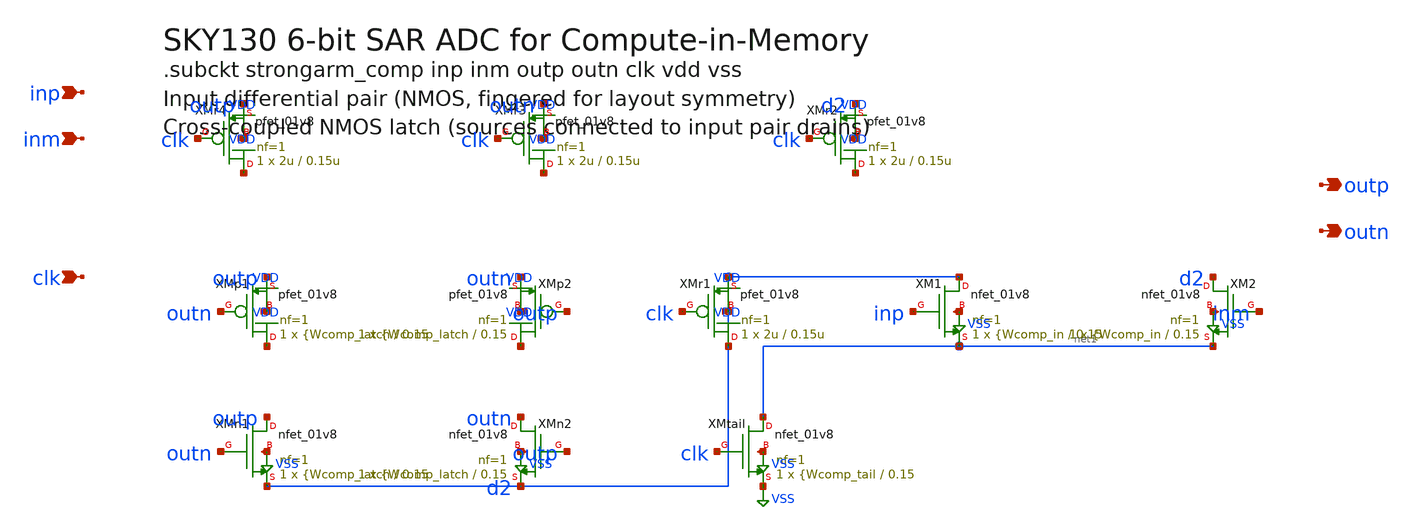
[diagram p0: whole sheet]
** sch_path: data/sch/cim_adc.sch
**.subckt cim_adc inp inm outp outn clk
*.ipin inp
*.ipin inm
*.opin outp
*.opin outn
*.ipin clk
XXMtail net1 clk VSS VSS sky130_fd_pr__nfet_01v8 L=0.15 W={Wcomp_tail nf=1 ad='int((1 + 1)/2) * {Wcomp_tail / 1 * 0.29'
+ as='int((1 + 2)/2) * {Wcomp_tail / 1 * 0.29' pd='2*int((1 + 1)/2) * ({Wcomp_tail / 1 + 0.29)' ps='2*int((1 + 2)/2) * ({Wcomp_tail
+ / 1 + 0.29)' nrd='0.29 / {Wcomp_tail ' nrs='0.29 / {Wcomp_tail ' sa=0 sb=0 sd=0 mult=1 m=1
XXM1 d2 inp net1 VSS sky130_fd_pr__nfet_01v8 L=0.15 W={Wcomp_in nf=1 ad='int((1 + 1)/2) * {Wcomp_in /
+ 1 * 0.29' as='int((1 + 2)/2) * {Wcomp_in / 1 * 0.29' pd='2*int((1 + 1)/2) * ({Wcomp_in / 1 + 0.29)' ps='2*int((1
+ + 2)/2) * ({Wcomp_in / 1 + 0.29)' nrd='0.29 / {Wcomp_in ' nrs='0.29 / {Wcomp_in ' sa=0 sb=0 sd=0 mult=1
+ m=1
XXM2 d2 inm net1 VSS sky130_fd_pr__nfet_01v8 L=0.15 W={Wcomp_in nf=1 ad='int((1 + 1)/2) * {Wcomp_in / 1 * 0.29'
+ as='int((1 + 2)/2) * {Wcomp_in / 1 * 0.29' pd='2*int((1 + 1)/2) * ({Wcomp_in / 1 + 0.29)' ps='2*int((1 + 2)/2) * ({Wcomp_in
+ / 1 + 0.29)' nrd='0.29 / {Wcomp_in ' nrs='0.29 / {Wcomp_in ' sa=0 sb=0 sd=0 mult=1 m=1
XXMr1 d2 clk d2 d2 sky130_fd_pr__pfet_01v8 L=0.15u W=2u nf=1 ad='int((nf+1)/2) * W/nf * 0.29' as='int((nf+2)/2)
+ * W/nf * 0.29' pd='2*int((nf+1)/2) * (W/nf + 0.29)' ps='2*int((nf+2)/2) * (W/nf + 0.29)' nrd='0.29 /
+ W' nrs='0.29 / W' sa=0 sb=0 sd=0 mult=1 m=1
XXMr2 VDD clk d2 VDD sky130_fd_pr__pfet_01v8 L=0.15u W=2u nf=1 ad='int((nf+1)/2) * W/nf * 0.29' as='int((nf+2)/2)
+ * W/nf * 0.29' pd='2*int((nf+1)/2) * (W/nf + 0.29)' ps='2*int((nf+2)/2) * (W/nf + 0.29)' nrd='0.29 /
+ W' nrs='0.29 / W' sa=0 sb=0 sd=0 mult=1 m=1
XXMr3 VDD clk outn VDD sky130_fd_pr__pfet_01v8 L=0.15u W=2u nf=1 ad='int((nf+1)/2) * W/nf * 0.29' as='int((nf+2)/2)
+ * W/nf * 0.29' pd='2*int((nf+1)/2) * (W/nf + 0.29)' ps='2*int((nf+2)/2) * (W/nf + 0.29)' nrd='0.29 /
+ W' nrs='0.29 / W' sa=0 sb=0 sd=0 mult=1 m=1
XXMr4 VDD clk outp VDD sky130_fd_pr__pfet_01v8 L=0.15u W=2u nf=1 ad='int((nf+1)/2) * W/nf * 0.29' as='int((nf+2)/2)
+ * W/nf * 0.29' pd='2*int((nf+1)/2) * (W/nf + 0.29)' ps='2*int((nf+2)/2) * (W/nf + 0.29)' nrd='0.29 /
+ W' nrs='0.29 / W' sa=0 sb=0 sd=0 mult=1 m=1
XXMp1 VDD outn outp VDD sky130_fd_pr__pfet_01v8 L=0.15 W={Wcomp_latch nf=1 ad='int((nf+1)/2) * W/nf * 0.29'
+ as='int((nf+2)/2) * W/nf * 0.29' pd='2*int((nf+1)/2) * (W/nf + 0.29)' ps='2*int((nf+2)/2) * (W/nf + 0.29)'
+ nrd='0.29 / W' nrs='0.29 / W' sa=0 sb=0 sd=0 mult=1 m=1
XXMp2 VDD outp outn VDD sky130_fd_pr__pfet_01v8 L=0.15 W={Wcomp_latch nf=1 ad='int((nf+1)/2) * W/nf *
+ 0.29' as='int((nf+2)/2) * W/nf * 0.29' pd='2*int((nf+1)/2) * (W/nf + 0.29)' ps='2*int((nf+2)/2) * (W/nf
+ + 0.29)' nrd='0.29 / W' nrs='0.29 / W' sa=0 sb=0 sd=0 mult=1 m=1
XXMn1 outp outn d2 VSS sky130_fd_pr__nfet_01v8 L=0.15 W={Wcomp_latch nf=1 ad='int((1 + 1)/2) * {Wcomp_latch
+ / 1 * 0.29' as='int((1 + 2)/2) * {Wcomp_latch / 1 * 0.29' pd='2*int((1 + 1)/2) * ({Wcomp_latch / 1 +
+ 0.29)' ps='2*int((1 + 2)/2) * ({Wcomp_latch / 1 + 0.29)' nrd='0.29 / {Wcomp_latch ' nrs='0.29 / {Wcomp_latch '
+ sa=0 sb=0 sd=0 mult=1 m=1
XXMn2 outn outp d2 VSS sky130_fd_pr__nfet_01v8 L=0.15 W={Wcomp_latch nf=1 ad='int((1 + 1)/2) * {Wcomp_latch / 1 * 0.29'
+ as='int((1 + 2)/2) * {Wcomp_latch / 1 * 0.29' pd='2*int((1 + 1)/2) * ({Wcomp_latch / 1 + 0.29)' ps='2*int((1 + 2)/2) * ({Wcomp_latch
+ / 1 + 0.29)' nrd='0.29 / {Wcomp_latch ' nrs='0.29 / {Wcomp_latch ' sa=0 sb=0 sd=0 mult=1 m=1
**.ends
.GLOBAL VSS
.GLOBAL VDD
.end
